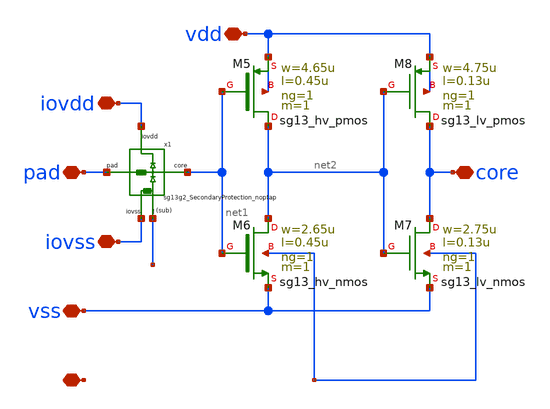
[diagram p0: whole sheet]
** sch_path: ihp-sg13g2/libs.tech/xschem/hm_stdcells/sg13g2_LevelDown_noptap.sch
**.subckt sg13g2_LevelDown_noptap iovdd vss core pad vdd iovss !
*.iopin iovdd
*.iopin vss
*.iopin core
*.iopin pad
*.iopin vdd
*.iopin iovss
*.iopin !
XM5 net2 net1 vdd vdd sg13_hv_pmos w=4.65u l=0.45u ng=1 m=1 mm_ok=1
XM6 net2 net1 vss ! sg13_hv_nmos w=2.65u l=0.45u ng=1 m=1 mm_ok=1
XM7 core net2 vss ! sg13_lv_nmos w=2.75u l=0.13u ng=1 m=1 mm_ok=1
XM8 core net2 vdd vdd sg13_lv_pmos w=4.75u l=0.13u ng=1 m=1 mm_ok=1
x1 net1 iovdd iovss pad ! sg13g2_SecondaryProtection_noptap
**.ends

* expanding   symbol:  hm_stdcells/sg13g2_SecondaryProtection_noptap.sym # of pins=5
** sym_path: ihp-sg13g2/libs.tech/xschem/hm_stdcells/sg13g2_SecondaryProtection_noptap.sym
** sch_path: ihp-sg13g2/libs.tech/xschem/hm_stdcells/sg13g2_SecondaryProtection_noptap.sch
.subckt sg13g2_SecondaryProtection_noptap core iovdd iovss pad !
*.iopin iovss
*.iopin core
*.iopin pad
*.iopin iovdd
*.iopin !
XD1 core iovdd dpantenna l=4.98u w=0.64u
XD2 ! core dantenna l=3.1u w=0.64u
XR1 core pad sub! rppd w=1e-6 l=2e-6 m=1 b=0 mm_ok=1
.ends

.end
